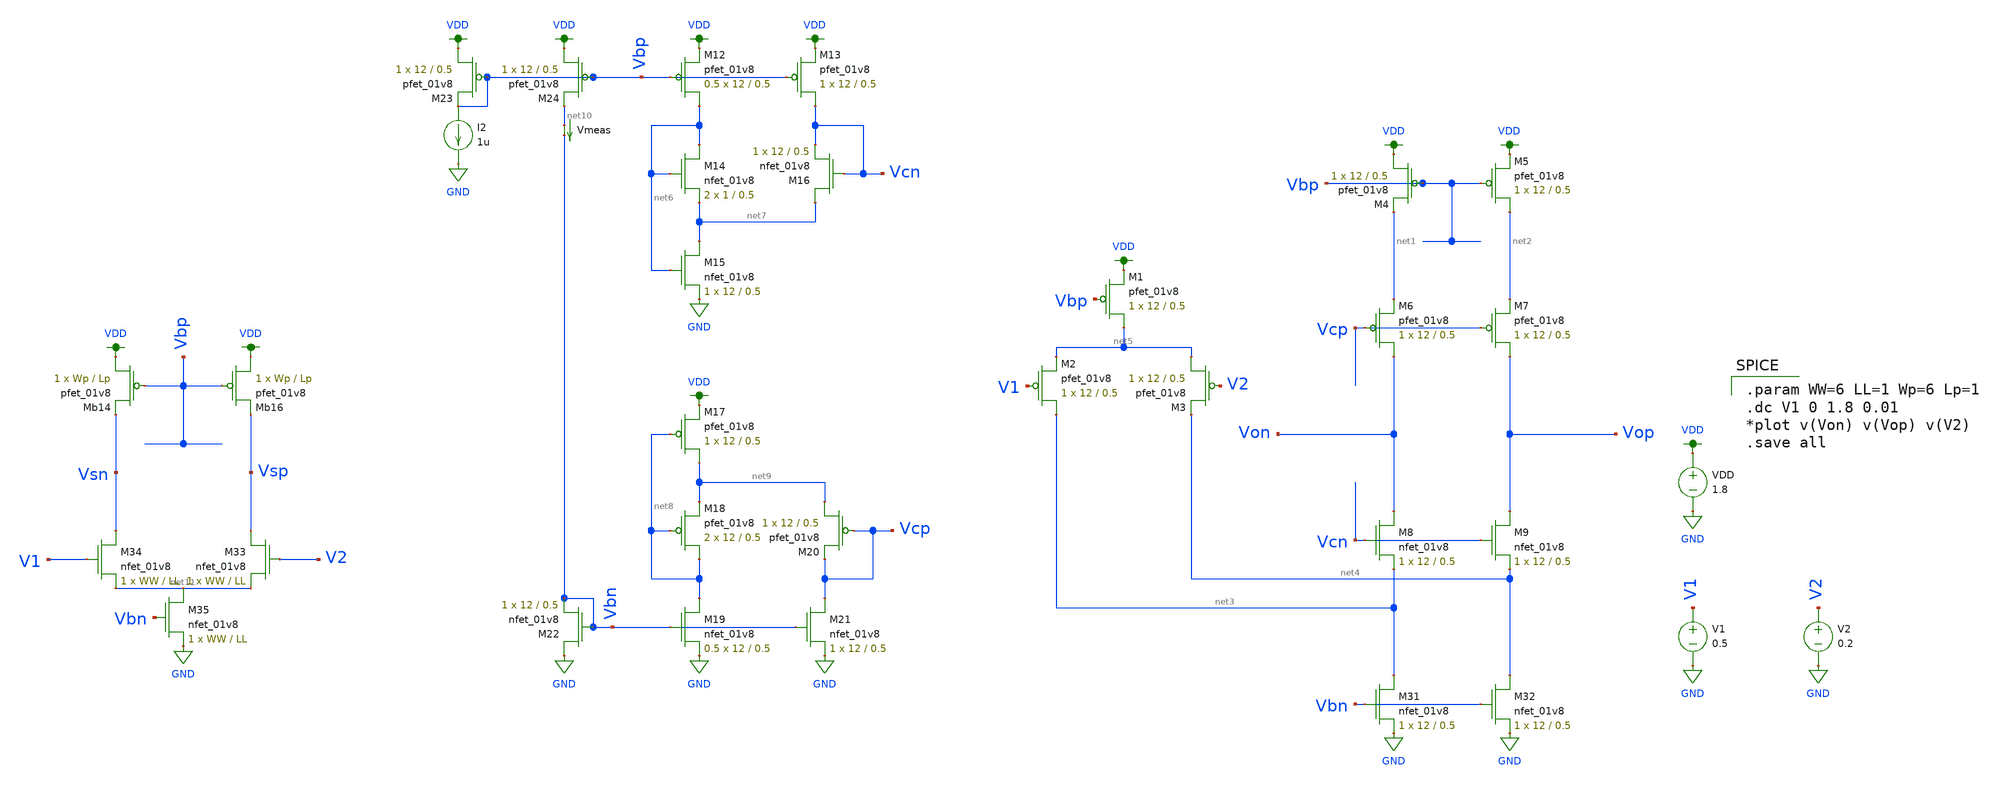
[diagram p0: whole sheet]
** sch_path: schematic/test/folded_cascode_FD.sch
**.subckt folded_cascode_FD
XM1 net5 Vbp VDD VDD sky130_fd_pr__pfet_01v8 L=0.5 W=12 nf=1 ad='int((nf+1)/2) * W/nf * 0.29' as='int((nf+2)/2) * W/nf * 0.29'
+ pd='2*int((nf+1)/2) * (W/nf + 0.29)' ps='2*int((nf+2)/2) * (W/nf + 0.29)' nrd='0.29 / W' nrs='0.29 / W'
+ sa=0 sb=0 sd=0 mult=1 m=1
XM2 net3 V1 net5 VDD sky130_fd_pr__pfet_01v8 L=0.5 W=12 nf=1 ad='int((nf+1)/2) * W/nf * 0.29' as='int((nf+2)/2) * W/nf * 0.29'
+ pd='2*int((nf+1)/2) * (W/nf + 0.29)' ps='2*int((nf+2)/2) * (W/nf + 0.29)' nrd='0.29 / W' nrs='0.29 / W'
+ sa=0 sb=0 sd=0 mult=1 m=1
XM3 net5 V2 net4 VDD sky130_fd_pr__pfet_01v8 L=0.5 W=12 nf=1 ad='int((nf+1)/2) * W/nf * 0.29' as='int((nf+2)/2) * W/nf * 0.29'
+ pd='2*int((nf+1)/2) * (W/nf + 0.29)' ps='2*int((nf+2)/2) * (W/nf + 0.29)' nrd='0.29 / W' nrs='0.29 / W'
+ sa=0 sb=0 sd=0 mult=1 m=1
XM4 VDD Vbp net1 VDD sky130_fd_pr__pfet_01v8 L=0.5 W=12 nf=1 ad='int((nf+1)/2) * W/nf * 0.29' as='int((nf+2)/2) * W/nf * 0.29'
+ pd='2*int((nf+1)/2) * (W/nf + 0.29)' ps='2*int((nf+2)/2) * (W/nf + 0.29)' nrd='0.29 / W' nrs='0.29 / W'
+ sa=0 sb=0 sd=0 mult=1 m=1
XM5 net2 Vbp VDD VDD sky130_fd_pr__pfet_01v8 L=0.5 W=12 nf=1 ad='int((nf+1)/2) * W/nf * 0.29' as='int((nf+2)/2) * W/nf * 0.29'
+ pd='2*int((nf+1)/2) * (W/nf + 0.29)' ps='2*int((nf+2)/2) * (W/nf + 0.29)' nrd='0.29 / W' nrs='0.29 / W'
+ sa=0 sb=0 sd=0 mult=1 m=1
XM6 Von Vcp net1 VDD sky130_fd_pr__pfet_01v8 L=0.5 W=12 nf=1 ad='int((nf+1)/2) * W/nf * 0.29' as='int((nf+2)/2) * W/nf * 0.29'
+ pd='2*int((nf+1)/2) * (W/nf + 0.29)' ps='2*int((nf+2)/2) * (W/nf + 0.29)' nrd='0.29 / W' nrs='0.29 / W'
+ sa=0 sb=0 sd=0 mult=1 m=1
XM7 Vop Vcp net2 VDD sky130_fd_pr__pfet_01v8 L=0.5 W=12 nf=1 ad='int((nf+1)/2) * W/nf * 0.29' as='int((nf+2)/2) * W/nf * 0.29'
+ pd='2*int((nf+1)/2) * (W/nf + 0.29)' ps='2*int((nf+2)/2) * (W/nf + 0.29)' nrd='0.29 / W' nrs='0.29 / W'
+ sa=0 sb=0 sd=0 mult=1 m=1
XM8 Von Vcn net3 GND sky130_fd_pr__nfet_01v8 L=0.5 W=12 nf=1 ad='int((nf+1)/2) * W/nf * 0.29' as='int((nf+2)/2) * W/nf * 0.29'
+ pd='2*int((nf+1)/2) * (W/nf + 0.29)' ps='2*int((nf+2)/2) * (W/nf + 0.29)' nrd='0.29 / W' nrs='0.29 / W'
+ sa=0 sb=0 sd=0 mult=1 m=1
XM9 Vop Vcn net4 GND sky130_fd_pr__nfet_01v8 L=0.5 W=12 nf=1 ad='int((nf+1)/2) * W/nf * 0.29' as='int((nf+2)/2) * W/nf * 0.29'
+ pd='2*int((nf+1)/2) * (W/nf + 0.29)' ps='2*int((nf+2)/2) * (W/nf + 0.29)' nrd='0.29 / W' nrs='0.29 / W'
+ sa=0 sb=0 sd=0 mult=1 m=1
XM12 net6 Vbp VDD VDD sky130_fd_pr__pfet_01v8 L=0.5 W=12 nf=1 ad='int((nf+1)/2) * W/nf * 0.29' as='int((nf+2)/2) * W/nf * 0.29'
+ pd='2*int((nf+1)/2) * (W/nf + 0.29)' ps='2*int((nf+2)/2) * (W/nf + 0.29)' nrd='0.29 / W' nrs='0.29 / W'
+ sa=0 sb=0 sd=0 mult=0.5 m=0.5
XM13 Vcn Vbp VDD VDD sky130_fd_pr__pfet_01v8 L=0.5 W=12 nf=1 ad='int((nf+1)/2) * W/nf * 0.29' as='int((nf+2)/2) * W/nf * 0.29'
+ pd='2*int((nf+1)/2) * (W/nf + 0.29)' ps='2*int((nf+2)/2) * (W/nf + 0.29)' nrd='0.29 / W' nrs='0.29 / W'
+ sa=0 sb=0 sd=0 mult=1 m=1
XM14 net6 net6 net7 GND sky130_fd_pr__nfet_01v8 L=0.5 W=1 nf=1 ad='int((nf+1)/2) * W/nf * 0.29' as='int((nf+2)/2) * W/nf * 0.29'
+ pd='2*int((nf+1)/2) * (W/nf + 0.29)' ps='2*int((nf+2)/2) * (W/nf + 0.29)' nrd='0.29 / W' nrs='0.29 / W'
+ sa=0 sb=0 sd=0 mult=2 m=2
XM15 net7 net6 GND GND sky130_fd_pr__nfet_01v8 L=0.5 W=12 nf=1 ad='int((nf+1)/2) * W/nf * 0.29' as='int((nf+2)/2) * W/nf * 0.29'
+ pd='2*int((nf+1)/2) * (W/nf + 0.29)' ps='2*int((nf+2)/2) * (W/nf + 0.29)' nrd='0.29 / W' nrs='0.29 / W'
+ sa=0 sb=0 sd=0 mult=1 m=1
XM16 net7 Vcn Vcn GND sky130_fd_pr__nfet_01v8 L=0.5 W=12 nf=1 ad='int((nf+1)/2) * W/nf * 0.29' as='int((nf+2)/2) * W/nf * 0.29'
+ pd='2*int((nf+1)/2) * (W/nf + 0.29)' ps='2*int((nf+2)/2) * (W/nf + 0.29)' nrd='0.29 / W' nrs='0.29 / W'
+ sa=0 sb=0 sd=0 mult=1 m=1
XM17 net9 net8 VDD VDD sky130_fd_pr__pfet_01v8 L=0.5 W=12 nf=1 ad='int((nf+1)/2) * W/nf * 0.29' as='int((nf+2)/2) * W/nf * 0.29'
+ pd='2*int((nf+1)/2) * (W/nf + 0.29)' ps='2*int((nf+2)/2) * (W/nf + 0.29)' nrd='0.29 / W' nrs='0.29 / W'
+ sa=0 sb=0 sd=0 mult=1 m=1
XM18 net8 net8 net9 VDD sky130_fd_pr__pfet_01v8 L=0.5 W=12 nf=1 ad='int((nf+1)/2) * W/nf * 0.29' as='int((nf+2)/2) * W/nf * 0.29'
+ pd='2*int((nf+1)/2) * (W/nf + 0.29)' ps='2*int((nf+2)/2) * (W/nf + 0.29)' nrd='0.29 / W' nrs='0.29 / W'
+ sa=0 sb=0 sd=0 mult=2 m=2
XM19 net8 Vbn GND GND sky130_fd_pr__nfet_01v8 L=0.5 W=12 nf=1 ad='int((nf+1)/2) * W/nf * 0.29' as='int((nf+2)/2) * W/nf * 0.29'
+ pd='2*int((nf+1)/2) * (W/nf + 0.29)' ps='2*int((nf+2)/2) * (W/nf + 0.29)' nrd='0.29 / W' nrs='0.29 / W'
+ sa=0 sb=0 sd=0 mult=0.5 m=0.5
XM20 net9 Vcp Vcp VDD sky130_fd_pr__pfet_01v8 L=0.5 W=12 nf=1 ad='int((nf+1)/2) * W/nf * 0.29' as='int((nf+2)/2) * W/nf * 0.29'
+ pd='2*int((nf+1)/2) * (W/nf + 0.29)' ps='2*int((nf+2)/2) * (W/nf + 0.29)' nrd='0.29 / W' nrs='0.29 / W'
+ sa=0 sb=0 sd=0 mult=1 m=1
XM21 Vcp Vbn GND GND sky130_fd_pr__nfet_01v8 L=0.5 W=12 nf=1 ad='int((nf+1)/2) * W/nf * 0.29' as='int((nf+2)/2) * W/nf * 0.29'
+ pd='2*int((nf+1)/2) * (W/nf + 0.29)' ps='2*int((nf+2)/2) * (W/nf + 0.29)' nrd='0.29 / W' nrs='0.29 / W'
+ sa=0 sb=0 sd=0 mult=1 m=1
VDD VDD GND 1.8
V1 V1 GND 0.5
V2 V2 GND 0.2
XM22 GND Vbn Vbn GND sky130_fd_pr__nfet_01v8 L=0.5 W=12 nf=1 ad='int((nf+1)/2) * W/nf * 0.29' as='int((nf+2)/2) * W/nf * 0.29'
+ pd='2*int((nf+1)/2) * (W/nf + 0.29)' ps='2*int((nf+2)/2) * (W/nf + 0.29)' nrd='0.29 / W' nrs='0.29 / W'
+ sa=0 sb=0 sd=0 mult=1 m=1
XM23 VDD Vbp Vbp VDD sky130_fd_pr__pfet_01v8 L=0.5 W=12 nf=1 ad='int((nf+1)/2) * W/nf * 0.29' as='int((nf+2)/2) * W/nf * 0.29'
+ pd='2*int((nf+1)/2) * (W/nf + 0.29)' ps='2*int((nf+2)/2) * (W/nf + 0.29)' nrd='0.29 / W' nrs='0.29 / W'
+ sa=0 sb=0 sd=0 mult=1 m=1
I2 Vbp GND 1u
XM24 VDD Vbp net10 VDD sky130_fd_pr__pfet_01v8 L=0.5 W=12 nf=1 ad='int((nf+1)/2) * W/nf * 0.29' as='int((nf+2)/2) * W/nf * 0.29'
+ pd='2*int((nf+1)/2) * (W/nf + 0.29)' ps='2*int((nf+2)/2) * (W/nf + 0.29)' nrd='0.29 / W' nrs='0.29 / W'
+ sa=0 sb=0 sd=0 mult=1 m=1
Vmeas net10 Vbn 0
.save i(vmeas)
XM31 net3 Vbn GND GND sky130_fd_pr__nfet_01v8 L=0.5 W=12 nf=1 ad='int((nf+1)/2) * W/nf * 0.29' as='int((nf+2)/2) * W/nf * 0.29'
+ pd='2*int((nf+1)/2) * (W/nf + 0.29)' ps='2*int((nf+2)/2) * (W/nf + 0.29)' nrd='0.29 / W' nrs='0.29 / W'
+ sa=0 sb=0 sd=0 mult=1 m=1
XM32 net4 Vbn GND GND sky130_fd_pr__nfet_01v8 L=0.5 W=12 nf=1 ad='int((nf+1)/2) * W/nf * 0.29' as='int((nf+2)/2) * W/nf * 0.29'
+ pd='2*int((nf+1)/2) * (W/nf + 0.29)' ps='2*int((nf+2)/2) * (W/nf + 0.29)' nrd='0.29 / W' nrs='0.29 / W'
+ sa=0 sb=0 sd=0 mult=1 m=1
XM33 Vsp V2 net11 GND sky130_fd_pr__nfet_01v8 L=LL W=WW nf=1 ad='int((nf+1)/2) * W/nf * 0.29' as='int((nf+2)/2) * W/nf * 0.29'
+ pd='2*int((nf+1)/2) * (W/nf + 0.29)' ps='2*int((nf+2)/2) * (W/nf + 0.29)' nrd='0.29 / W' nrs='0.29 / W'
+ sa=0 sb=0 sd=0 mult=1 m=1
XM34 Vsn V1 net11 GND sky130_fd_pr__nfet_01v8 L=LL W=WW nf=1 ad='int((nf+1)/2) * W/nf * 0.29' as='int((nf+2)/2) * W/nf * 0.29'
+ pd='2*int((nf+1)/2) * (W/nf + 0.29)' ps='2*int((nf+2)/2) * (W/nf + 0.29)' nrd='0.29 / W' nrs='0.29 / W'
+ sa=0 sb=0 sd=0 mult=1 m=1
XM35 net11 Vbn GND GND sky130_fd_pr__nfet_01v8 L=LL W=WW nf=1 ad='int((nf+1)/2) * W/nf * 0.29' as='int((nf+2)/2) * W/nf * 0.29'
+ pd='2*int((nf+1)/2) * (W/nf + 0.29)' ps='2*int((nf+2)/2) * (W/nf + 0.29)' nrd='0.29 / W' nrs='0.29 / W'
+ sa=0 sb=0 sd=0 mult=1 m=1
XMb14 VDD Vbp Vsn VDD sky130_fd_pr__pfet_01v8 L=Lp W=Wp nf=1 ad='int((nf+1)/2) * W/nf * 0.29' as='int((nf+2)/2) * W/nf * 0.29'
+ pd='2*int((nf+1)/2) * (W/nf + 0.29)' ps='2*int((nf+2)/2) * (W/nf + 0.29)' nrd='0.29 / W' nrs='0.29 / W'
+ sa=0 sb=0 sd=0 mult=1 m=1
XMb16 VDD Vbp Vsp VDD sky130_fd_pr__pfet_01v8 L=Lp W=Wp nf=1 ad='int((nf+1)/2) * W/nf * 0.29' as='int((nf+2)/2) * W/nf * 0.29'
+ pd='2*int((nf+1)/2) * (W/nf + 0.29)' ps='2*int((nf+2)/2) * (W/nf + 0.29)' nrd='0.29 / W' nrs='0.29 / W'
+ sa=0 sb=0 sd=0 mult=1 m=1
**** begin user architecture code

.param WW=6 LL=1 Wp=6 Lp=1
.dc V1 0 1.8 0.01
*plot v(Von) v(Vop) v(V2)
.save all


.option wnflag=1
.param MC_SWITCH=0.0
.lib ~/skywater/skywater-pdk/libraries/sky130_fd_pr_ngspice/latest/models/sky130.lib.spice tt

**** end user architecture code
**.ends
.GLOBAL VDD
.GLOBAL GND
.end
